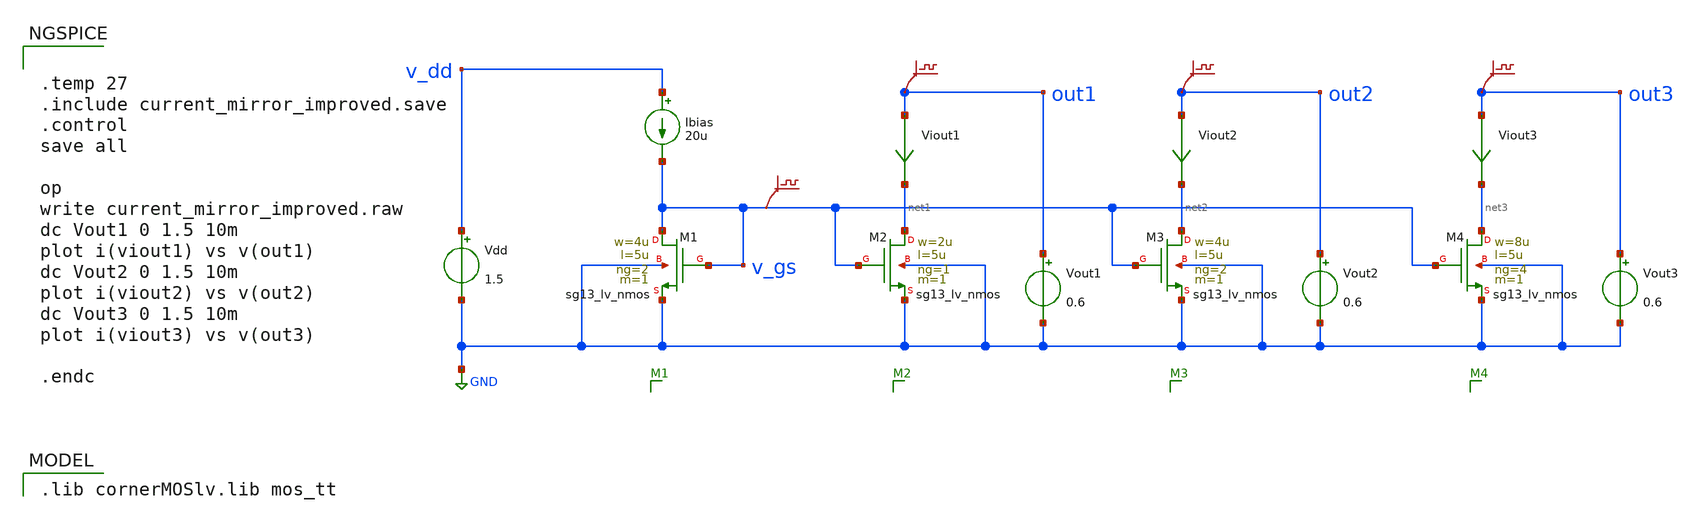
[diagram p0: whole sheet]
** sch_path: xschem/current_mirror_improved.sch
* (c) 2024-2025 Harald Pretl, Apache-2.0 license
**.subckt current_mirror_improved
Vdd v_dd GND 1.5
XM1 v_gs v_gs GND GND sg13_lv_nmos w=4u l=5u ng=2 m=1 mm_ok=1
Ibias v_dd v_gs 20u
XM2 net1 v_gs GND GND sg13_lv_nmos w=2u l=5u ng=1 m=1 mm_ok=1
XM3 net2 v_gs GND GND sg13_lv_nmos w=4u l=5u ng=2 m=1 mm_ok=1
XM4 net3 v_gs GND GND sg13_lv_nmos w=8u l=5u ng=4 m=1 mm_ok=1
Vout1 out1 GND 0.6
Vout2 out2 GND 0.6
Vout3 out3 GND 0.6
.save v(out1)
.save v(out2)
.save v(out3)
.save v(v_gs)
Viout1 out1 net1 0
.save i(viout1)
Viout2 out2 net2 0
.save i(viout2)
Viout3 out3 net3 0
.save i(viout3)
**** begin user architecture code
 .lib cornerMOSlv.lib mos_tt



.temp 27
.include current_mirror_improved.save
.control
save all

op
write current_mirror_improved.raw
dc Vout1 0 1.5 10m
plot i(viout1) vs v(out1)
dc Vout2 0 1.5 10m
plot i(viout2) vs v(out2)
dc Vout3 0 1.5 10m
plot i(viout3) vs v(out3)

.endc


**** end user architecture code
**.ends
.GLOBAL GND
.end
